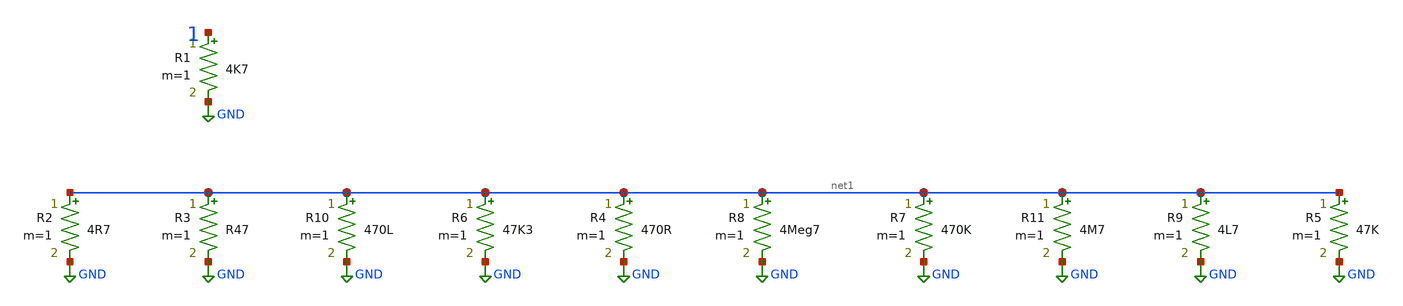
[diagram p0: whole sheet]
** sch_path: data/sch/aicas_RKM-R-1.sch
**.subckt aicas_RKM-R-1
R1 1 GND 4K7 m=1
R2 net1 GND 4R7 m=1
R3 net1 GND R47 m=1
R4 net1 GND 470R m=1
R5 net1 GND 47K m=1
R6 net1 GND 47K3 m=1
R7 net1 GND 470K m=1
R8 net1 GND 4Meg7 m=1
R9 net1 GND 4L7 m=1
R10 net1 GND 470L m=1
R11 net1 GND 4M7 m=1
**.ends
.GLOBAL GND
.end
